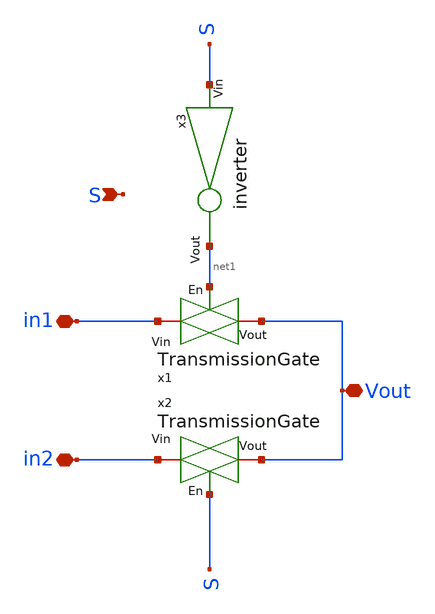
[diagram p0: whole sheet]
** sch_path: xschem/Final/Analogmux2.sch
**.subckt Analogmux2 in1 in2 Vout S
*.iopin in1
*.iopin in2
*.iopin Vout
*.ipin S
x1 in1 net1 Vout TransmissionGate
x2 in2 S Vout TransmissionGate
x3 net1 S inverter
**.ends
.end
